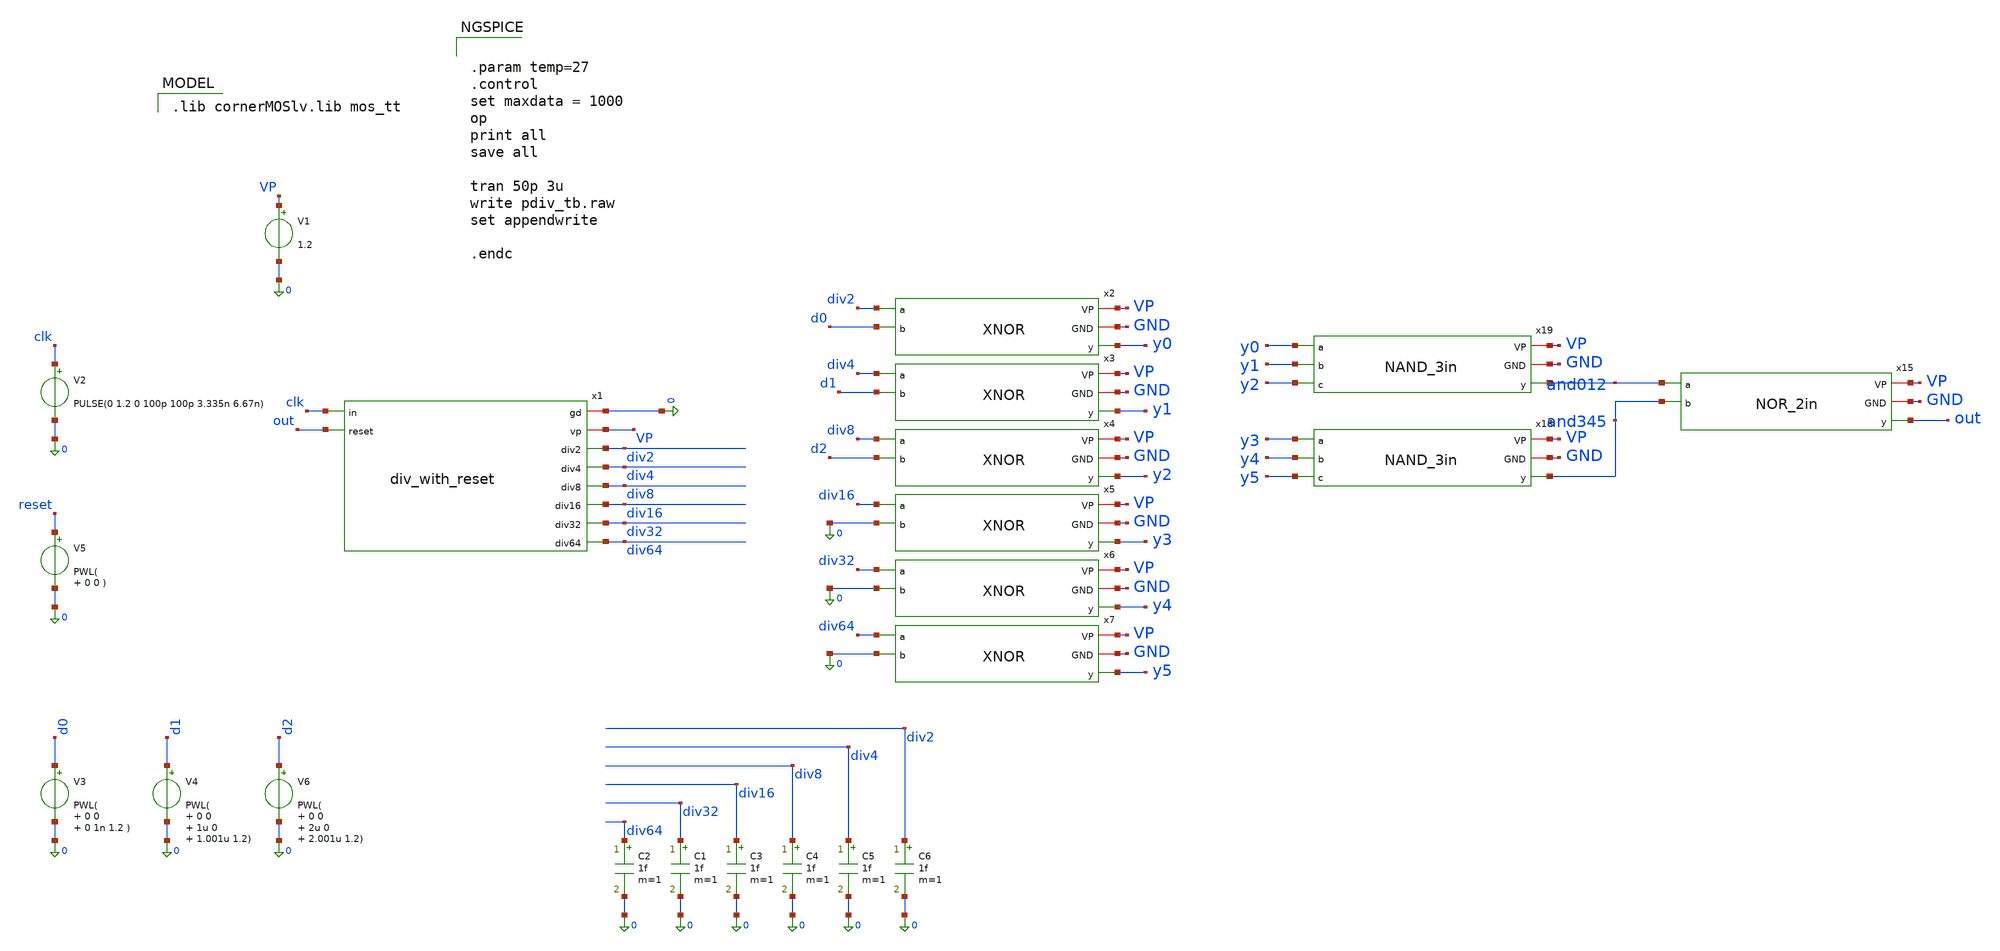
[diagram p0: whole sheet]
** sch_path: divider/tb/pdiv_tb.sch
**.subckt pdiv_tb
V1 VP 0 1.2
V2 clk 0 PULSE(0 1.2 0 100p 100p 3.335n 6.67n)
x1 0 VP clk out div2 div4 div8 div16 div32 div64 div_with_reset
V3 d0 0 PWL( 0 0 0 1n 1.2 )
V4 d1 0 PWL( 0 0 1u 0 1.001u 1.2)
V6 d2 0 PWL( 0 0 2u 0 2.001u 1.2)
V5 reset 0 PWL( 0 0 )
C2 div64 0 1f m=1
C1 div32 0 1f m=1
C3 div16 0 1f m=1
C4 div8 0 1f m=1
C5 div4 0 1f m=1
C6 div2 0 1f m=1
x2 VP GND div2 y0 d0 XNOR
x3 VP GND div4 y1 d1 XNOR
x4 VP GND div8 y2 d2 XNOR
x5 VP GND div16 y3 0 XNOR
x6 VP GND div32 y4 0 XNOR
x7 VP GND div64 y5 0 XNOR
x18 VP GND y3 and345 y4 y5 NAND_3in
x19 VP GND y0 and012 y1 y2 NAND_3in
x15 VP GND and012 out and345 NOR_2in
**** begin user architecture code
 .lib cornerMOSlv.lib mos_tt



.param temp=27
.control
set maxdata = 1000
op
print all
save all

tran 50p 3u
write pdiv_tb.raw
set appendwrite

.endc


**** end user architecture code
**.ends
.end
